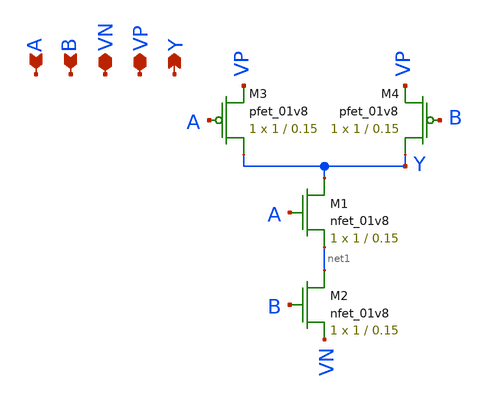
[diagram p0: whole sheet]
** sch_path: xschem/logic_gates/nand.sch
**.subckt nand VP VN A B Y
*.iopin VP
*.iopin VN
*.ipin A
*.ipin B
*.opin Y
XM1 Y A net1 GND sky130_fd_pr__nfet_01v8 L=0.15 W=1 nf=1 ad='int((nf+1)/2) * W/nf * 0.29' as='int((nf+2)/2) * W/nf * 0.29'
+ pd='2*int((nf+1)/2) * (W/nf + 0.29)' ps='2*int((nf+2)/2) * (W/nf + 0.29)' nrd='0.29 / W' nrs='0.29 / W'
+ sa=0 sb=0 sd=0 mult=1 m=1
XM2 net1 B VN GND sky130_fd_pr__nfet_01v8 L=0.15 W=1 nf=1 ad='int((nf+1)/2) * W/nf * 0.29' as='int((nf+2)/2) * W/nf * 0.29'
+ pd='2*int((nf+1)/2) * (W/nf + 0.29)' ps='2*int((nf+2)/2) * (W/nf + 0.29)' nrd='0.29 / W' nrs='0.29 / W'
+ sa=0 sb=0 sd=0 mult=1 m=1
XM3 Y A VP VDD sky130_fd_pr__pfet_01v8 L=0.15 W=1 nf=1 ad='int((nf+1)/2) * W/nf * 0.29' as='int((nf+2)/2) * W/nf * 0.29'
+ pd='2*int((nf+1)/2) * (W/nf + 0.29)' ps='2*int((nf+2)/2) * (W/nf + 0.29)' nrd='0.29 / W' nrs='0.29 / W'
+ sa=0 sb=0 sd=0 mult=1 m=1
XM4 Y B VP VDD sky130_fd_pr__pfet_01v8 L=0.15 W=1 nf=1 ad='int((nf+1)/2) * W/nf * 0.29' as='int((nf+2)/2) * W/nf * 0.29'
+ pd='2*int((nf+1)/2) * (W/nf + 0.29)' ps='2*int((nf+2)/2) * (W/nf + 0.29)' nrd='0.29 / W' nrs='0.29 / W'
+ sa=0 sb=0 sd=0 mult=1 m=1
**.ends
.end
